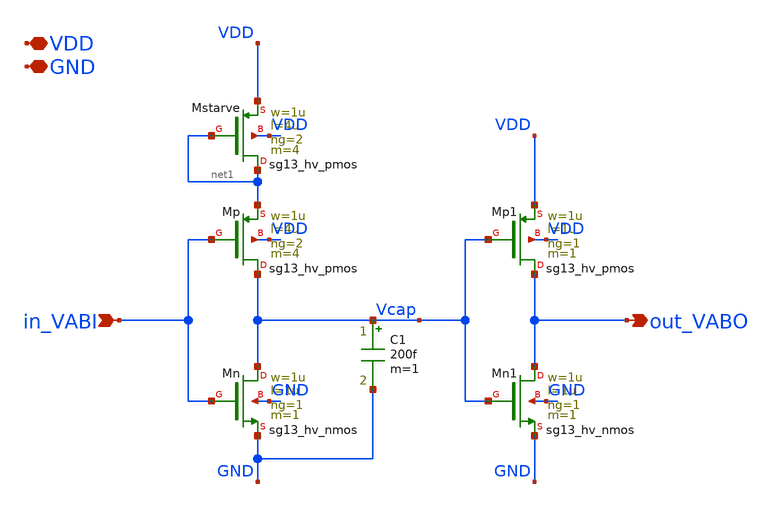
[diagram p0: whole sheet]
** sch_path: xschem/ncs-dpi-adexp/xschem/pulse_extender.sch
**.subckt pulse_extender in_VABI out_VABO VDD GND
*.ipin in_VABI
*.opin out_VABO
*.iopin VDD
*.iopin GND
XMstarve net1 net1 VDD VDD sg13_hv_pmos w=1u l=4u ng=2 m=4 mm_ok=1
XMp Vcap in_VABI net1 VDD sg13_hv_pmos w=1u l=4u ng=2 m=4 mm_ok=1
XMn Vcap in_VABI GND GND sg13_hv_nmos w=1u l=1u ng=1 m=1 mm_ok=1
C1 Vcap GND 200f m=1
XMp1 out_VABO Vcap VDD VDD sg13_hv_pmos w=1u l=1u ng=1 m=1 mm_ok=1
XMn1 out_VABO Vcap GND GND sg13_hv_nmos w=1u l=1u ng=1 m=1 mm_ok=1
**.ends
.end
